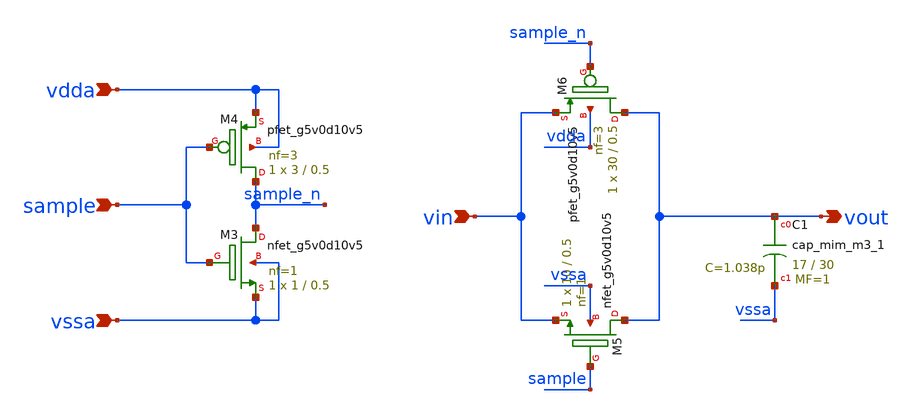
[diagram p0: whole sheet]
** sch_path: xschem/sample_hold.sch
**.subckt sample_hold vout vdda vssa vin sample
*.opin vout
*.ipin vdda
*.ipin vssa
*.ipin vin
*.ipin sample
XM5 vout sample vin vssa sky130_fd_pr__nfet_g5v0d10v5 L=0.5 W=10 nf=1 ad='int((nf+1)/2) * W/nf * 0.29'
+ as='int((nf+2)/2) * W/nf * 0.29' pd='2*int((nf+1)/2) * (W/nf + 0.29)' ps='2*int((nf+2)/2) * (W/nf + 0.29)'
+ nrd='0.29 / W' nrs='0.29 / W' sa=0 sb=0 sd=0 mult=1 m=1
XM6 vout sample_n vin vdda sky130_fd_pr__pfet_g5v0d10v5 L=0.5 W=30 nf=3 ad='int((nf+1)/2) * W/nf * 0.29'
+ as='int((nf+2)/2) * W/nf * 0.29' pd='2*int((nf+1)/2) * (W/nf + 0.29)' ps='2*int((nf+2)/2) * (W/nf + 0.29)'
+ nrd='0.29 / W' nrs='0.29 / W' sa=0 sb=0 sd=0 mult=1 m=1
XM3 sample_n sample vssa vssa sky130_fd_pr__nfet_g5v0d10v5 L=0.5 W=1 nf=1 ad='int((nf+1)/2) * W/nf * 0.29'
+ as='int((nf+2)/2) * W/nf * 0.29' pd='2*int((nf+1)/2) * (W/nf + 0.29)' ps='2*int((nf+2)/2) * (W/nf + 0.29)'
+ nrd='0.29 / W' nrs='0.29 / W' sa=0 sb=0 sd=0 mult=1 m=1
XM4 sample_n sample vdda vdda sky130_fd_pr__pfet_g5v0d10v5 L=0.5 W=3 nf=3 ad='int((nf+1)/2) * W/nf * 0.29'
+ as='int((nf+2)/2) * W/nf * 0.29' pd='2*int((nf+1)/2) * (W/nf + 0.29)' ps='2*int((nf+2)/2) * (W/nf + 0.29)'
+ nrd='0.29 / W' nrs='0.29 / W' sa=0 sb=0 sd=0 mult=1 m=1
XC1 vout vssa sky130_fd_pr__cap_mim_m3_1 W=17 L=30 MF=1 m=1
**.ends
.end
